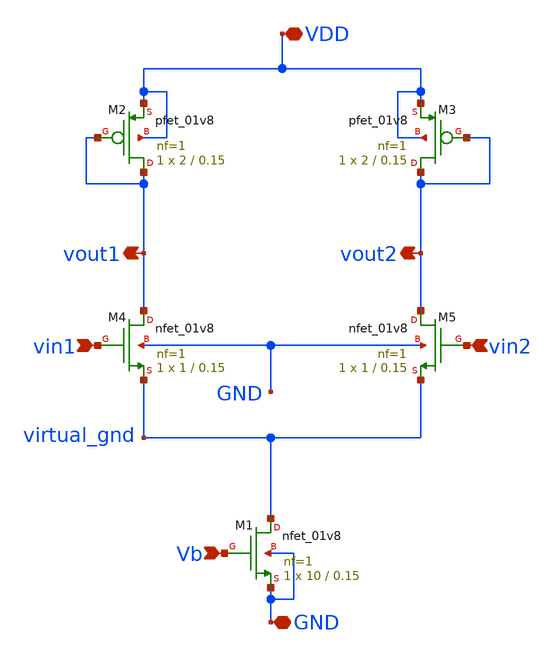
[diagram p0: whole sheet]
** sch_path: xschem/diff_amp.sch
**.subckt diff_amp Vb vout2 vout1 vin2 vin1 GND VDD
*.ipin Vb
*.opin vout2
*.opin vout1
*.ipin vin2
*.ipin vin1
*.iopin GND
*.iopin VDD
XM1 virtual_gnd Vb GND GND sky130_fd_pr__nfet_01v8 L=0.15 W=10 nf=1 ad='int((nf+1)/2) * W/nf * 0.29'
+ as='int((nf+2)/2) * W/nf * 0.29' pd='2*int((nf+1)/2) * (W/nf + 0.29)' ps='2*int((nf+2)/2) * (W/nf + 0.29)'
+ nrd='0.29 / W' nrs='0.29 / W' sa=0 sb=0 sd=0 mult=1 m=1
XM2 vout1 vout1 VDD VDD sky130_fd_pr__pfet_01v8 L=0.15 W=2 nf=1 ad='int((nf+1)/2) * W/nf * 0.29' as='int((nf+2)/2) * W/nf * 0.29'
+ pd='2*int((nf+1)/2) * (W/nf + 0.29)' ps='2*int((nf+2)/2) * (W/nf + 0.29)' nrd='0.29 / W' nrs='0.29 / W'
+ sa=0 sb=0 sd=0 mult=1 m=1
XM3 vout2 vout2 VDD VDD sky130_fd_pr__pfet_01v8 L=0.15 W=2 nf=1 ad='int((nf+1)/2) * W/nf * 0.29' as='int((nf+2)/2) * W/nf * 0.29'
+ pd='2*int((nf+1)/2) * (W/nf + 0.29)' ps='2*int((nf+2)/2) * (W/nf + 0.29)' nrd='0.29 / W' nrs='0.29 / W'
+ sa=0 sb=0 sd=0 mult=1 m=1
XM4 vout1 vin1 virtual_gnd GND sky130_fd_pr__nfet_01v8 L=0.15 W=1 nf=1 ad='int((nf+1)/2) * W/nf * 0.29'
+ as='int((nf+2)/2) * W/nf * 0.29' pd='2*int((nf+1)/2) * (W/nf + 0.29)' ps='2*int((nf+2)/2) * (W/nf + 0.29)'
+ nrd='0.29 / W' nrs='0.29 / W' sa=0 sb=0 sd=0 mult=1 m=1
XM5 vout2 vin2 virtual_gnd GND sky130_fd_pr__nfet_01v8 L=0.15 W=1 nf=1 ad='int((nf+1)/2) * W/nf * 0.29'
+ as='int((nf+2)/2) * W/nf * 0.29' pd='2*int((nf+1)/2) * (W/nf + 0.29)' ps='2*int((nf+2)/2) * (W/nf + 0.29)'
+ nrd='0.29 / W' nrs='0.29 / W' sa=0 sb=0 sd=0 mult=1 m=1
**.ends
.end
